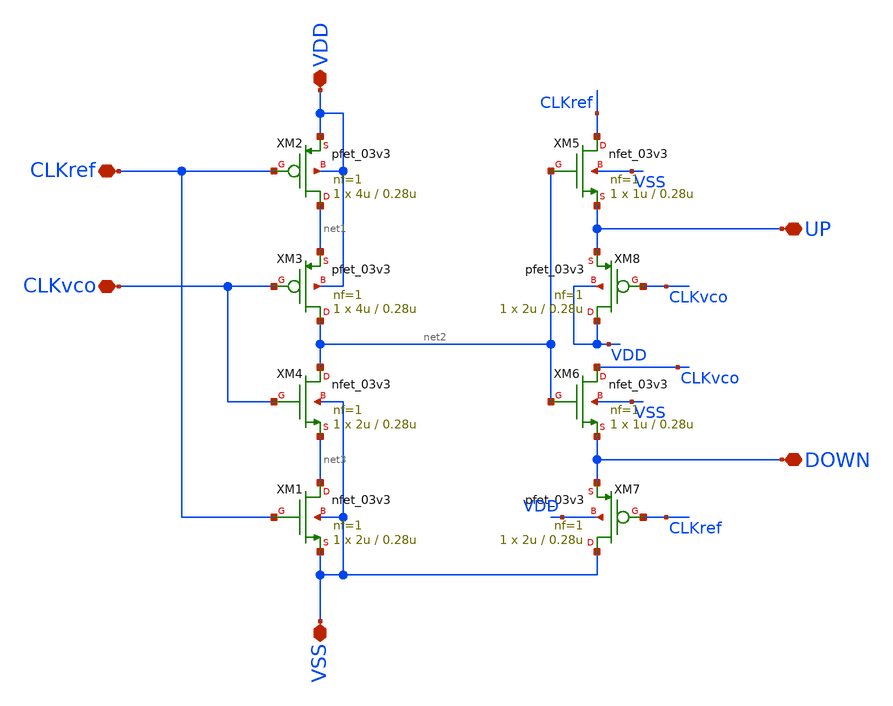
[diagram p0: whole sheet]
** sch_path: designs/libs/qw_core_analog_pkedit/untitled.sch
**.subckt untitled CLKref CLKvco VSS VDD UP DOWN
*.iopin CLKref
*.iopin CLKvco
*.iopin VSS
*.iopin VDD
*.iopin UP
*.iopin DOWN
XM1 net3 CLKref VSS VSS nfet_03v3 L=0.28u W=2u nf=1 ad='int((nf+1)/2) * W/nf * 0.18u' as='int((nf+2)/2) * W/nf * 0.18u'
+ pd='2*int((nf+1)/2) * (W/nf + 0.18u)' ps='2*int((nf+2)/2) * (W/nf + 0.18u)' nrd='0.18u / W' nrs='0.18u / W'
+ sa=0 sb=0 sd=0 m=1
XM2 net1 CLKref VDD VDD pfet_03v3 L=0.28u W=4u nf=1 ad='int((nf+1)/2) * W/nf * 0.18u' as='int((nf+2)/2) * W/nf * 0.18u'
+ pd='2*int((nf+1)/2) * (W/nf + 0.18u)' ps='2*int((nf+2)/2) * (W/nf + 0.18u)' nrd='0.18u / W' nrs='0.18u / W'
+ sa=0 sb=0 sd=0 m=1
XM3 net2 CLKvco net1 VDD pfet_03v3 L=0.28u W=4u nf=1 ad='int((nf+1)/2) * W/nf * 0.18u' as='int((nf+2)/2) * W/nf * 0.18u'
+ pd='2*int((nf+1)/2) * (W/nf + 0.18u)' ps='2*int((nf+2)/2) * (W/nf + 0.18u)' nrd='0.18u / W' nrs='0.18u / W'
+ sa=0 sb=0 sd=0 m=1
XM4 net2 CLKvco net3 VSS nfet_03v3 L=0.28u W=2u nf=1 ad='int((nf+1)/2) * W/nf * 0.18u' as='int((nf+2)/2) * W/nf * 0.18u'
+ pd='2*int((nf+1)/2) * (W/nf + 0.18u)' ps='2*int((nf+2)/2) * (W/nf + 0.18u)' nrd='0.18u / W' nrs='0.18u / W'
+ sa=0 sb=0 sd=0 m=1
XM5 CLKref net2 UP VSS nfet_03v3 L=0.28u W=1u nf=1 ad='int((nf+1)/2) * W/nf * 0.18u' as='int((nf+2)/2) * W/nf * 0.18u'
+ pd='2*int((nf+1)/2) * (W/nf + 0.18u)' ps='2*int((nf+2)/2) * (W/nf + 0.18u)' nrd='0.18u / W' nrs='0.18u / W'
+ sa=0 sb=0 sd=0 m=1
XM6 CLKvco net2 DOWN VSS nfet_03v3 L=0.28u W=1u nf=1 ad='int((nf+1)/2) * W/nf * 0.18u' as='int((nf+2)/2) * W/nf * 0.18u'
+ pd='2*int((nf+1)/2) * (W/nf + 0.18u)' ps='2*int((nf+2)/2) * (W/nf + 0.18u)' nrd='0.18u / W' nrs='0.18u / W'
+ sa=0 sb=0 sd=0 m=1
XM7 VSS CLKref DOWN VDD pfet_03v3 L=0.28u W=2u nf=1 ad='int((nf+1)/2) * W/nf * 0.18u' as='int((nf+2)/2) * W/nf * 0.18u'
+ pd='2*int((nf+1)/2) * (W/nf + 0.18u)' ps='2*int((nf+2)/2) * (W/nf + 0.18u)' nrd='0.18u / W' nrs='0.18u / W'
+ sa=0 sb=0 sd=0 m=1
XM8 VDD CLKvco UP VDD pfet_03v3 L=0.28u W=2u nf=1 ad='int((nf+1)/2) * W/nf * 0.18u' as='int((nf+2)/2) * W/nf * 0.18u'
+ pd='2*int((nf+1)/2) * (W/nf + 0.18u)' ps='2*int((nf+2)/2) * (W/nf + 0.18u)' nrd='0.18u / W' nrs='0.18u / W'
+ sa=0 sb=0 sd=0 m=1
**.ends
.end
